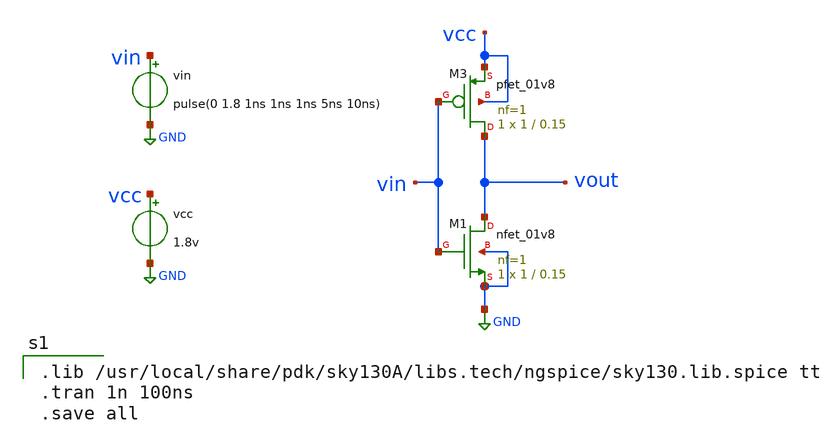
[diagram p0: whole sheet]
** sch_path: 02 - Schematic Level Simulations/CMOS_inverter.sch
**.subckt CMOS_inverter
vcc vcc GND 1.8v
vin vin GND pulse(0 1.8 1ns 1ns 1ns 5ns 10ns)
XM1 vout vin GND GND sky130_fd_pr__nfet_01v8 L=0.15 W=1 nf=1 ad='int((nf+1)/2) * W/nf * 0.29' as='int((nf+2)/2) * W/nf * 0.29'
+ pd='2*int((nf+1)/2) * (W/nf + 0.29)' ps='2*int((nf+2)/2) * (W/nf + 0.29)' nrd='0.29 / W' nrs='0.29 / W'
+ sa=0 sb=0 sd=0 mult=1 m=1
XM3 vout vin vcc vcc sky130_fd_pr__pfet_01v8 L=0.15 W=1 nf=1 ad='int((nf+1)/2) * W/nf * 0.29' as='int((nf+2)/2) * W/nf * 0.29'
+ pd='2*int((nf+1)/2) * (W/nf + 0.29)' ps='2*int((nf+2)/2) * (W/nf + 0.29)' nrd='0.29 / W' nrs='0.29 / W'
+ sa=0 sb=0 sd=0 mult=1 m=1
**** begin user architecture code

.lib /usr/local/share/pdk/sky130A/libs.tech/ngspice/sky130.lib.spice tt
.tran 1n 100ns
.save all

**** end user architecture code
**.ends
.GLOBAL GND
.end
